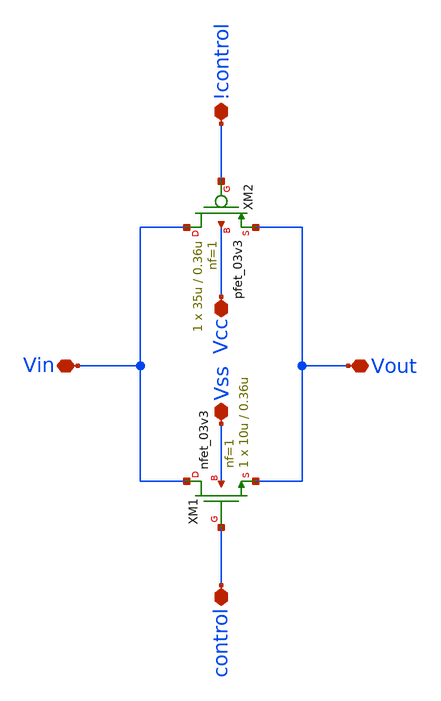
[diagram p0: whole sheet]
** sch_path: Array Components/Switch Array/T Gate/T_gate.sch
**.subckt T_gate Vout Vin !control control Vss Vcc
*.iopin Vout
*.iopin Vin
*.iopin !control
*.iopin control
*.iopin Vss
*.iopin Vcc
XM1 Vin control Vout Vss nfet_03v3 L=0.36u W=10u nf=1 ad='int((nf+1)/2) * W/nf * 0.18u' as='int((nf+2)/2) * W/nf * 0.18u'
+ pd='2*int((nf+1)/2) * (W/nf + 0.18u)' ps='2*int((nf+2)/2) * (W/nf + 0.18u)' nrd='0.18u / W' nrs='0.18u / W'
+ sa=0 sb=0 sd=0 m=1
XM2 Vin !control Vout Vcc pfet_03v3 L=0.36u W=35u nf=1 ad='int((nf+1)/2) * W/nf * 0.18u' as='int((nf+2)/2) * W/nf * 0.18u'
+ pd='2*int((nf+1)/2) * (W/nf + 0.18u)' ps='2*int((nf+2)/2) * (W/nf + 0.18u)' nrd='0.18u / W' nrs='0.18u / W'
+ sa=0 sb=0 sd=0 m=1
**.ends
.end
